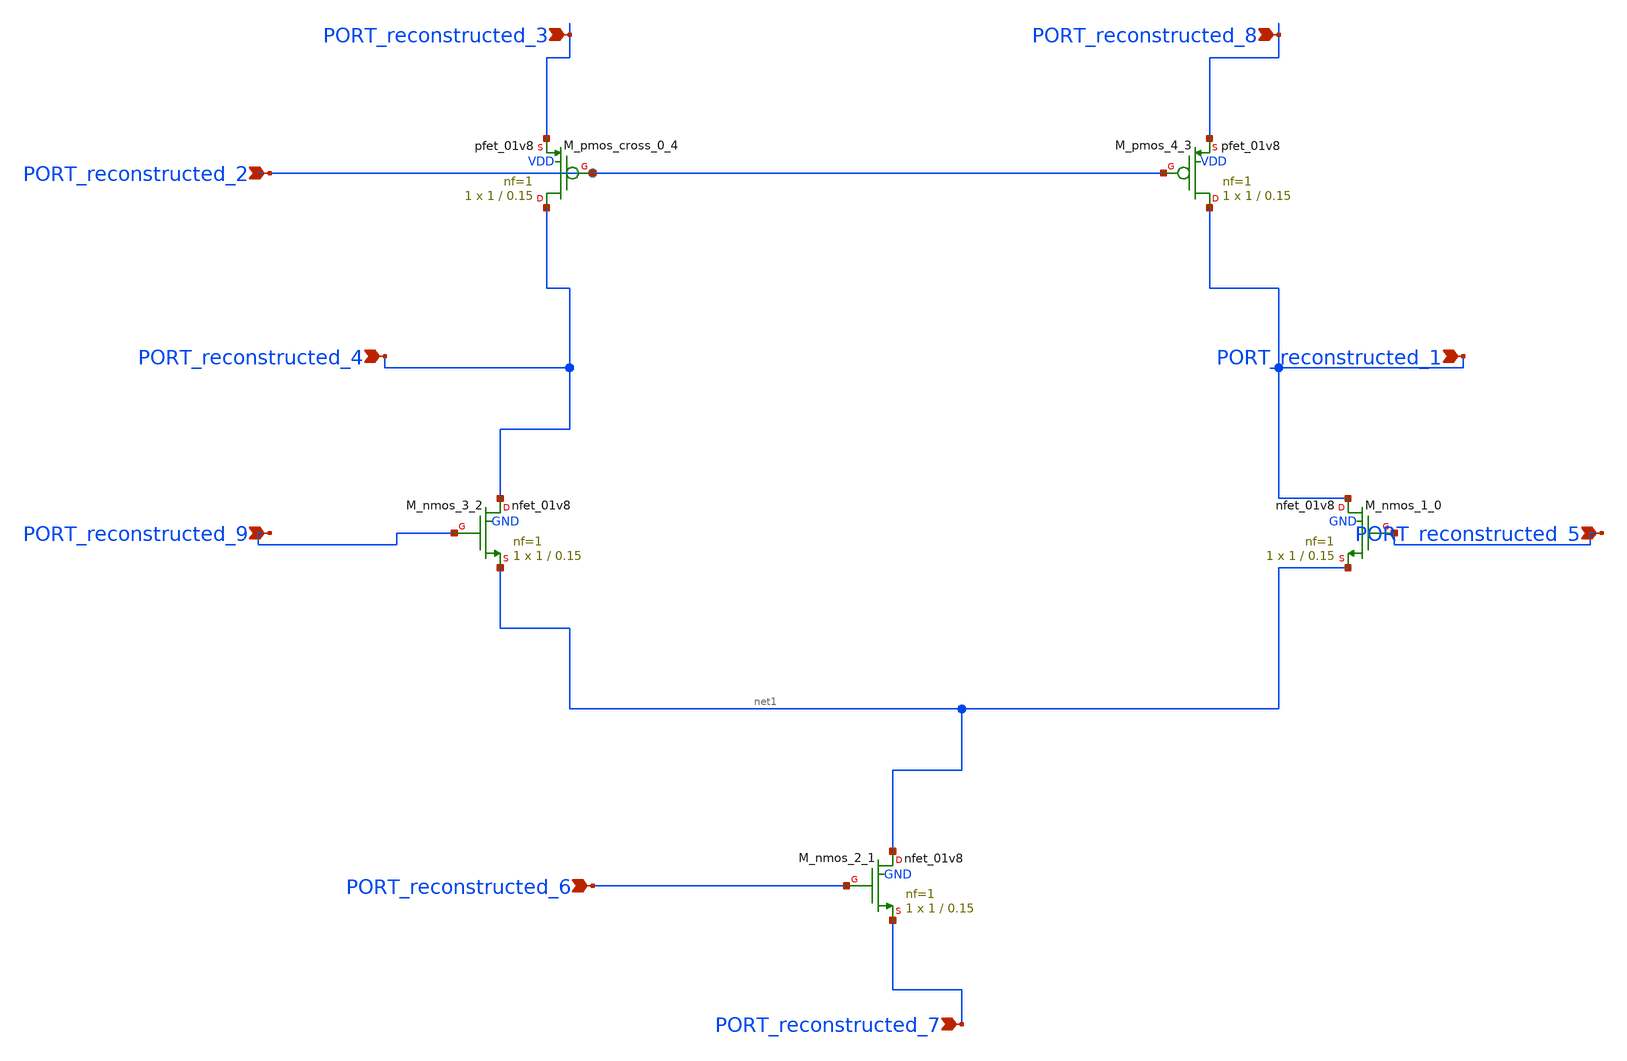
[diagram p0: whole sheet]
** sch_path: schematics/p07_fig12_sl_ota.sch
**.subckt p07_fig12_sl_ota PORT_reconstructed_4 PORT_reconstructed_5 PORT_reconstructed_6
*+ PORT_reconstructed_7 PORT_reconstructed_8 PORT_reconstructed_3 PORT_reconstructed_2 PORT_reconstructed_9
*+ PORT_reconstructed_1
*.ipin PORT_reconstructed_4
*.ipin PORT_reconstructed_5
*.ipin PORT_reconstructed_6
*.ipin PORT_reconstructed_7
*.ipin PORT_reconstructed_8
*.ipin PORT_reconstructed_3
*.ipin PORT_reconstructed_2
*.ipin PORT_reconstructed_9
*.ipin PORT_reconstructed_1
XM_nmos_1_0 PORT_reconstructed_1 PORT_reconstructed_5 net1 GND sky130_fd_pr__nfet_01v8 L=0.15 W=1 nf=1
+ ad='int((1 + 1)/2) * 1 / 1 * 0.29' as='int((1 + 2)/2) * 1 / 1 * 0.29' pd='2*int((1 + 1)/2) * (1 / 1 + 0.29)'
+ ps='2*int((1 + 2)/2) * (1 / 1 + 0.29)' nrd='0.29 / 1 ' nrs='0.29 / 1 ' sa=0 sb=0 sd=0 mult=1 m=1
XM_nmos_2_1 net1 PORT_reconstructed_6 PORT_reconstructed_7 GND sky130_fd_pr__nfet_01v8 L=0.15 W=1 nf=1
+ ad='int((1 + 1)/2) * 1 / 1 * 0.29' as='int((1 + 2)/2) * 1 / 1 * 0.29' pd='2*int((1 + 1)/2) * (1 / 1 + 0.29)'
+ ps='2*int((1 + 2)/2) * (1 / 1 + 0.29)' nrd='0.29 / 1 ' nrs='0.29 / 1 ' sa=0 sb=0 sd=0 mult=1 m=1
XM_nmos_3_2 PORT_reconstructed_4 PORT_reconstructed_9 net1 GND sky130_fd_pr__nfet_01v8 L=0.15 W=1 nf=1
+ ad='int((1 + 1)/2) * 1 / 1 * 0.29' as='int((1 + 2)/2) * 1 / 1 * 0.29' pd='2*int((1 + 1)/2) * (1 / 1 + 0.29)'
+ ps='2*int((1 + 2)/2) * (1 / 1 + 0.29)' nrd='0.29 / 1 ' nrs='0.29 / 1 ' sa=0 sb=0 sd=0 mult=1 m=1
XM_pmos_4_3 PORT_reconstructed_1 PORT_reconstructed_2 PORT_reconstructed_8 VDD sky130_fd_pr__pfet_01v8
+ L=0.15 W=1 nf=1 ad='int((1 + 1)/2) * 1 / 1 * 0.29' as='int((1 + 2)/2) * 1 / 1 * 0.29' pd='2*int((1 + 1)/2) * (1 / 1 + 0.29)'
+ ps='2*int((1 + 2)/2) * (1 / 1 + 0.29)' nrd='0.29 / 1 ' nrs='0.29 / 1 ' sa=0 sb=0 sd=0 mult=1 m=1
XM_pmos_cross_0_4 PORT_reconstructed_4 PORT_reconstructed_2 PORT_reconstructed_3 VDD sky130_fd_pr__pfet_01v8
+ L=0.15 W=1 nf=1 ad='int((1 + 1)/2) * 1 / 1 * 0.29' as='int((1 + 2)/2) * 1 / 1 * 0.29' pd='2*int((1 + 1)/2) * (1 / 1 + 0.29)'
+ ps='2*int((1 + 2)/2) * (1 / 1 + 0.29)' nrd='0.29 / 1 ' nrs='0.29 / 1 ' sa=0 sb=0 sd=0 mult=1 m=1
**.ends
.end
